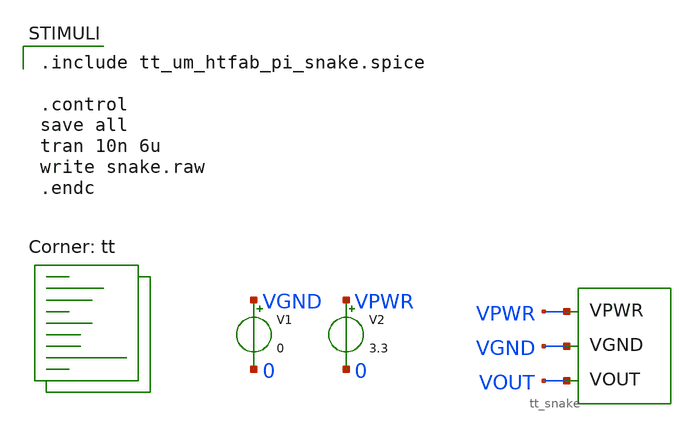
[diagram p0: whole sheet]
** sch_path: custom_gds/tt_um_htfab_pi_snake/sim/tb.sch
**.subckt tb
V1 VGND 0 0
V2 VPWR 0 3.3
x1 0 0 0 VOUT 0 0 0 0 0 0 0 0 0 0 0 0 0 0 0 0 0 0 0 0 0 0 0 0 0 0 0 0 0 0 0 0 0 0 0 0 0 0 0 0 0 0 0
+ 0 0 0 0 0 VGND VPWR tt_um_htfab_pi_snake
**** begin user architecture code
.lib $::SKYWATER_MODELS/sky130.lib.spice tt

.include tt_um_htfab_pi_snake.spice

.control
save all
tran 10n 6u
write snake.raw
.endc

**** end user architecture code
**.ends
.end
